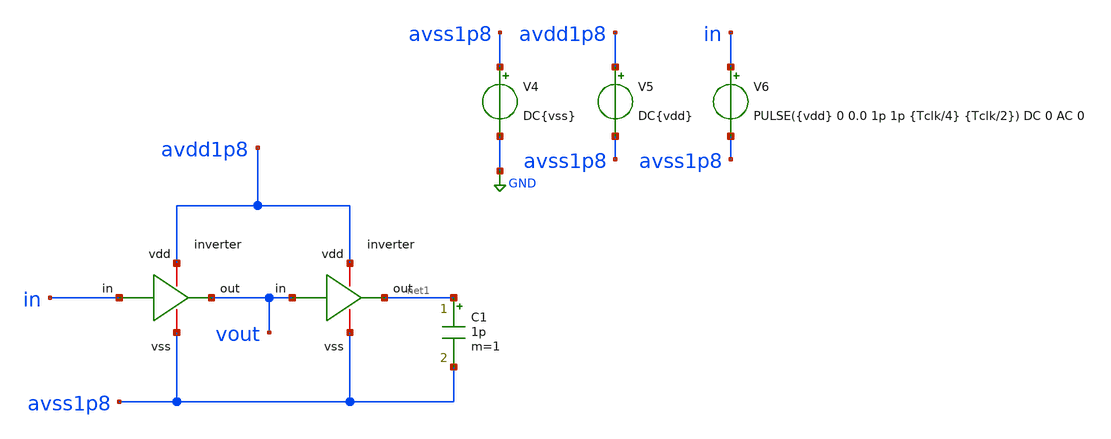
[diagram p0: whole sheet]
** sch_path: verification/testbenches/tb_inverter.sch
**.subckt tb_inverter
C1 net1 avss1p8 1p m=1
V4 avss1p8 GND DC{vss}
V5 avdd1p8 avss1p8 DC{vdd}
V6 in avss1p8 PULSE({vdd} 0 0.0 1p 1p {Tclk/4} {Tclk/2}) DC 0 AC 0
x2 avdd1p8 net1 vout avss1p8 inverter
x1 avdd1p8 vout in avss1p8 inverter
**** begin user architecture code


* Circuit Parameters
.param vdd = 1.2
.param vss = 0.0
.param Tclk = 10n
.options TEMP = 27.0
* Include Models - IHP SG13G2
.lib cornerMOSlv.lib mos_tt
* OP Parameters & Singals to save
.save all
*Simulations
.control
tran 0.01u 100n
setplot tran1
plot v(in) v(vout) + 1.2 v(vout)
set filetype = ascii
write dcsweep.raw
.endc
.end


**** end user architecture code
**.ends

* expanding   symbol:  blocks/inverter/schematic/inverter.sym # of pins=4
** sym_path: design/blocks/inverter/schematic/inverter.sym
** sch_path: design/blocks/inverter/schematic/inverter.sch
.subckt inverter vdd out in vss
*.iopin vdd
*.iopin out
*.iopin vss
*.iopin in
XM1 out in vss vss sky130_fd_pr__nfet_01v8 L=0.15 W=0.75 nf=1 ad='int((nf+1)/2) * W/nf * 0.29' as='int((nf+2)/2) * W/nf * 0.29'
+ pd='2*int((nf+1)/2) * (W/nf + 0.29)' ps='2*int((nf+2)/2) * (W/nf + 0.29)' nrd='0.29 / W' nrs='0.29 / W'
+ sa=0 sb=0 sd=0 mult=1 m=1
XM2 out in vdd vdd sky130_fd_pr__pfet_01v8 L=0.15 W=1.5 nf=1 ad='int((nf+1)/2) * W/nf * 0.29' as='int((nf+2)/2) * W/nf * 0.29'
+ pd='2*int((nf+1)/2) * (W/nf + 0.29)' ps='2*int((nf+2)/2) * (W/nf + 0.29)' nrd='0.29 / W' nrs='0.29 / W'
+ sa=0 sb=0 sd=0 mult=1 m=1
.ends

.GLOBAL GND
.end
